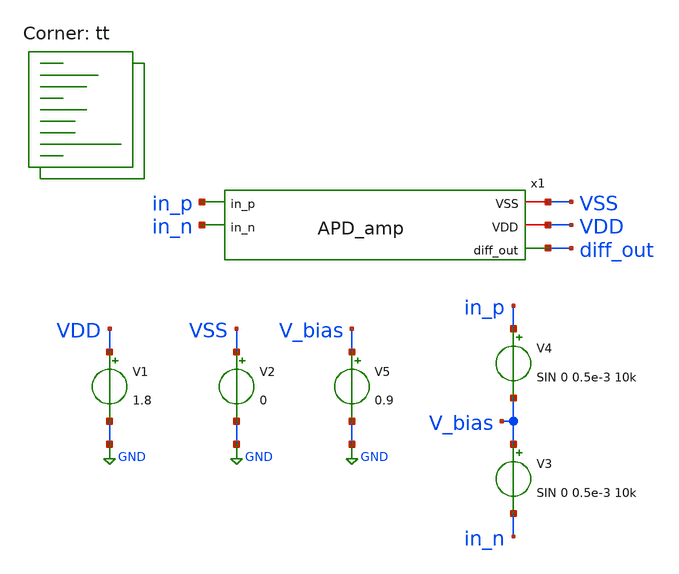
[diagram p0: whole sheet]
** sch_path: xschem/amp_test.sch
**.subckt amp_test
V1 VDD GND 1.8
V2 VSS GND 0
V3 V_bias in_n SIN 0 0.5e-3 10k
V4 in_p V_bias SIN 0 0.5e-3 10k
V5 V_bias GND 0.9
x1 in_p in_n VSS VDD diff_out APD_amp
**** begin user architecture code
.lib $::SKYWATER_MODELS/sky130.lib.spice tt



* ngspice commands
.options method=gear

.control
save all
ac dec 20 1 1e10
* tran 0.1u 100u 0
* plot diff_out in_p-in_n

* write amp_test.raw
.endc



**** end user architecture code
**.ends

* expanding   symbol:  APD_amp.sym # of pins=5
** sym_path: xschem/APD_amp.sym
** sch_path: xschem/APD_amp.sch
.subckt APD_amp in_p in_n VSS VDD diff_out
*.iopin VDD
*.ipin in_n
*.ipin in_p
*.opin diff_out
*.iopin VSS
XM3 net2 VDD VSS VSS sky130_fd_pr__nfet_01v8_lvt L=0.15 W=1 nf=1 ad='int((nf+1)/2) * W/nf * 0.29' as='int((nf+2)/2) * W/nf * 0.29'
+ pd='2*int((nf+1)/2) * (W/nf + 0.29)' ps='2*int((nf+2)/2) * (W/nf + 0.29)' nrd='0.29 / W' nrs='0.29 / W'
+ sa=0 sb=0 sd=0 mult=1 m=1
XM1 VDD VDD VSS VSS sky130_fd_pr__nfet_01v8_lvt L=0.15 W=1 nf=1 ad='int((nf+1)/2) * W/nf * 0.29' as='int((nf+2)/2) * W/nf * 0.29'
+ pd='2*int((nf+1)/2) * (W/nf + 0.29)' ps='2*int((nf+2)/2) * (W/nf + 0.29)' nrd='0.29 / W' nrs='0.29 / W'
+ sa=0 sb=0 sd=0 mult=1 m=1
XM2 VDD net1 net1 net3 sky130_fd_pr__pfet_01v8 L=0.15 W=1 nf=1 ad='int((nf+1)/2) * W/nf * 0.29' as='int((nf+2)/2) * W/nf * 0.29'
+ pd='2*int((nf+1)/2) * (W/nf + 0.29)' ps='2*int((nf+2)/2) * (W/nf + 0.29)' nrd='0.29 / W' nrs='0.29 / W'
+ sa=0 sb=0 sd=0 mult=1 m=1
XM5 VDD net1 diff_out net4 sky130_fd_pr__pfet_01v8 L=0.15 W=1 nf=1 ad='int((nf+1)/2) * W/nf * 0.29' as='int((nf+2)/2) * W/nf * 0.29'
+ pd='2*int((nf+1)/2) * (W/nf + 0.29)' ps='2*int((nf+2)/2) * (W/nf + 0.29)' nrd='0.29 / W' nrs='0.29 / W'
+ sa=0 sb=0 sd=0 mult=1 m=1
XM6 diff_out in_n net2 VSS sky130_fd_pr__nfet_01v8_lvt L=0.15 W=1 nf=1 ad='int((nf+1)/2) * W/nf * 0.29'
+ as='int((nf+2)/2) * W/nf * 0.29' pd='2*int((nf+1)/2) * (W/nf + 0.29)' ps='2*int((nf+2)/2) * (W/nf + 0.29)'
+ nrd='0.29 / W' nrs='0.29 / W' sa=0 sb=0 sd=0 mult=1 m=1
XM4 net1 in_p net2 VSS sky130_fd_pr__nfet_01v8_lvt L=0.15 W=1 nf=1 ad='int((nf+1)/2) * W/nf * 0.29' as='int((nf+2)/2) * W/nf * 0.29'
+ pd='2*int((nf+1)/2) * (W/nf + 0.29)' ps='2*int((nf+2)/2) * (W/nf + 0.29)' nrd='0.29 / W' nrs='0.29 / W'
+ sa=0 sb=0 sd=0 mult=1 m=1
.ends

.GLOBAL GND
.end
